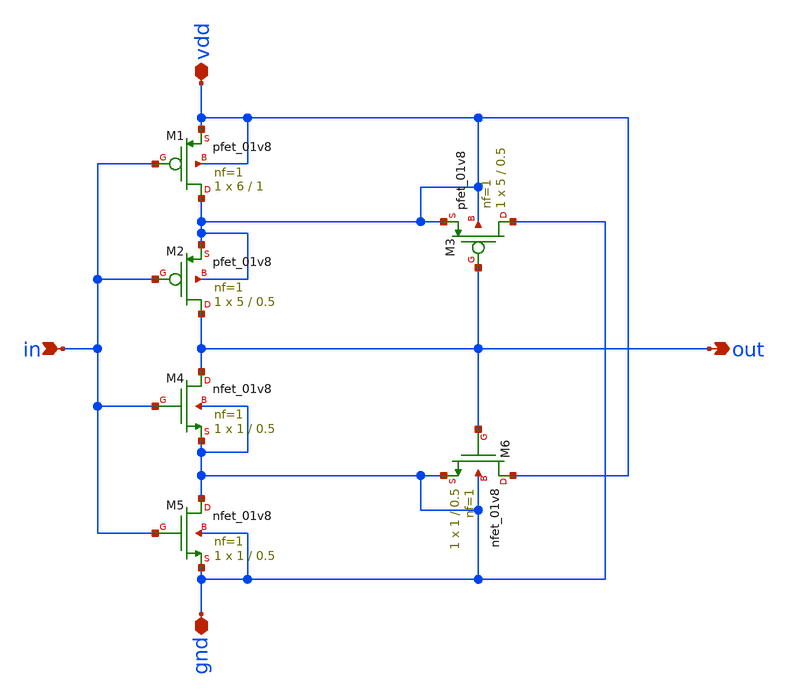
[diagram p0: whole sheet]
** sch_path: analog/mixer/schmidt-trigger.sch
**.subckt schmidt-trigger out in vdd gnd
*.opin out
*.ipin in
*.iopin vdd
*.iopin gnd
XM2 out in vdd vdd sky130_fd_pr__pfet_01v8 L=0.5 W=5 nf=1 ad='int((1 + 1)/2) * 5 / 1 * 0.29' as='int((1 + 2)/2) * 5 / 1 * 0.29'
+ pd='2*int((1 + 1)/2) * (5 / 1 + 0.29)' ps='2*int((1 + 2)/2) * (5 / 1 + 0.29)' nrd='0.29 / 5 ' nrs='0.29 / 5 '
+ sa=0 sb=0 sd=0 mult=1 m=1
XM1 vdd in vdd vdd sky130_fd_pr__pfet_01v8 L=1 W=6 nf=1 ad='int((1 + 1)/2) * 6 / 1 * 0.29' as='int((1 + 2)/2) * 6 / 1 * 0.29'
+ pd='2*int((1 + 1)/2) * (6 / 1 + 0.29)' ps='2*int((1 + 2)/2) * (6 / 1 + 0.29)' nrd='0.29 / 6 ' nrs='0.29 / 6 '
+ sa=0 sb=0 sd=0 mult=1 m=1
XM3 gnd out vdd vdd sky130_fd_pr__pfet_01v8 L=0.5 W=5 nf=1 ad='int((1 + 1)/2) * 5 / 1 * 0.29' as='int((1 + 2)/2) * 5 / 1 * 0.29'
+ pd='2*int((1 + 1)/2) * (5 / 1 + 0.29)' ps='2*int((1 + 2)/2) * (5 / 1 + 0.29)' nrd='0.29 / 5 ' nrs='0.29 / 5 '
+ sa=0 sb=0 sd=0 mult=1 m=1
XM4 out in gnd gnd sky130_fd_pr__nfet_01v8 L=0.5 W=1 nf=1 ad='int((1 + 1)/2) * 1 / 1 * 0.29' as='int((1 + 2)/2) * 1 / 1 * 0.29'
+ pd='2*int((1 + 1)/2) * (1 / 1 + 0.29)' ps='2*int((1 + 2)/2) * (1 / 1 + 0.29)' nrd='0.29 / 1 ' nrs='0.29 / 1 '
+ sa=0 sb=0 sd=0 mult=1 m=1
XM5 gnd in gnd gnd sky130_fd_pr__nfet_01v8 L=0.5 W=1 nf=1 ad='int((1 + 1)/2) * 1 / 1 * 0.29' as='int((1 + 2)/2) * 1 / 1 * 0.29'
+ pd='2*int((1 + 1)/2) * (1 / 1 + 0.29)' ps='2*int((1 + 2)/2) * (1 / 1 + 0.29)' nrd='0.29 / 1 ' nrs='0.29 / 1 '
+ sa=0 sb=0 sd=0 mult=1 m=1
XM6 vdd out gnd gnd sky130_fd_pr__nfet_01v8 L=0.5 W=1 nf=1 ad='int((1 + 1)/2) * 1 / 1 * 0.29' as='int((1 + 2)/2) * 1 / 1 * 0.29'
+ pd='2*int((1 + 1)/2) * (1 / 1 + 0.29)' ps='2*int((1 + 2)/2) * (1 / 1 + 0.29)' nrd='0.29 / 1 ' nrs='0.29 / 1 '
+ sa=0 sb=0 sd=0 mult=1 m=1
**.ends
.end
